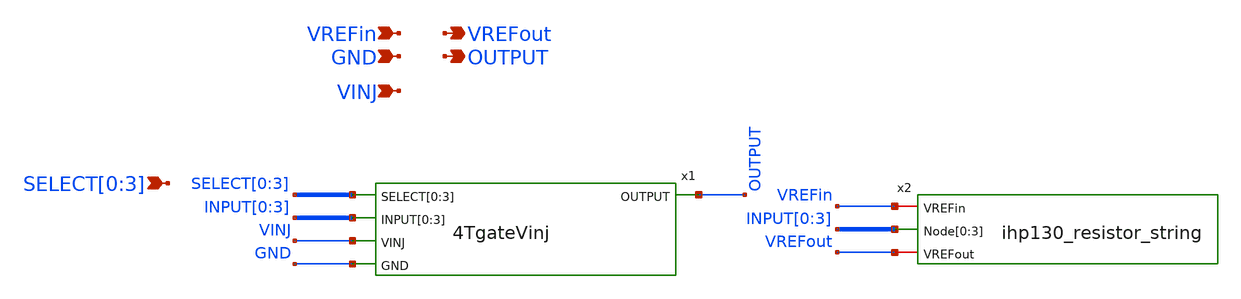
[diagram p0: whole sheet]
** sch_path: ihp130_cells/DAC_Cell/ihp130_DAC_cell.sch
**.subckt ihp130_DAC_cell GND VINJ SELECT[0],SELECT[1],SELECT[2],SELECT[3] VREFin VREFout OUTPUT
*.ipin GND
*.ipin VINJ
*.ipin SELECT[0],SELECT[1],SELECT[2],SELECT[3]
*.ipin VREFin
*.opin VREFout
*.opin OUTPUT
x1 SELECT[0] SELECT[1] SELECT[2] SELECT[3] OUTPUT INPUT[0] INPUT[1] INPUT[2] INPUT[3] VINJ GND
+ 4TgateVinj
x2 VREFin INPUT[0] INPUT[1] INPUT[2] INPUT[3] VREFout ihp130_resistor_string
**.ends

* expanding   symbol:  4TgateVinj/4TgateVinj.sym # of pins=5
** sym_path: ihp130_cells/4TgateVinj/4TgateVinj.sym
** sch_path: ihp130_cells/4TgateVinj/4TgateVinj.sch
.subckt 4TgateVinj SELECT[0] SELECT[1] SELECT[2] SELECT[3] OUTPUT INPUT[0] INPUT[1] INPUT[2]
+ INPUT[3] VINJ GND
*.ipin SELECT[0],SELECT[1],SELECT[2],SELECT[3]
*.ipin INPUT[0],INPUT[1],INPUT[2],INPUT[3]
*.ipin VINJ
*.ipin GND
*.opin OUTPUT
x1 SELECT[0] INPUT[0] VINJ GND OUTPUT ihp130_TgateVinj02
x2 SELECT[1] INPUT[1] VINJ GND OUTPUT ihp130_TgateVinj02
x3 SELECT[2] INPUT[2] VINJ GND OUTPUT ihp130_TgateVinj02
x4 SELECT[3] INPUT[3] VINJ GND OUTPUT ihp130_TgateVinj02
.ends


* expanding   symbol:  Resistor_String/ihp130_resistor_string.sym # of pins=3
** sym_path: ihp130_cells/Resistor_String/ihp130_resistor_string.sym
** sch_path: ihp130_cells/Resistor_String/ihp130_resistor_string.sch
.subckt ihp130_resistor_string VREFin Node[0] Node[1] Node[2] Node[3] VREFout
*.iopin VREFout
*.iopin VREFin
*.opin Node[0],Node[1],Node[2],Node[3]
XR8 VREFin Node[0] sub! rsil w=.59e-6 l=10e-6 m=1 mm_ok=1
XR1 Node[0] net1 sub! rsil w=.59e-6 l=10e-6 m=1 mm_ok=1
XR2 net1 Node[1] sub! rsil w=.59e-6 l=10e-6 m=1 mm_ok=1
XR3 Node[1] net2 sub! rsil w=.59e-6 l=10e-6 m=1 mm_ok=1
XR4 net2 Node[2] sub! rsil w=.59e-6 l=10e-6 m=1 mm_ok=1
XR5 Node[2] net3 sub! rsil w=.59e-6 l=10e-6 m=1 mm_ok=1
XR6 net3 Node[3] sub! rsil w=.59e-6 l=10e-6 m=1 mm_ok=1
XR7 Node[3] VREFout sub! rsil w=.59e-6 l=10e-6 m=1 mm_ok=1
.ends


* expanding   symbol:  TgateVinj02/ihp130_TgateVinj02.sym # of pins=5
** sym_path: ihp130_cells/TgateVinj02/ihp130_TgateVinj02.sym
** sch_path: ihp130_cells/TgateVinj02/ihp130_TgateVinj02.sch
.subckt ihp130_TgateVinj02 SELECT INPUT VINJ GND OUTPUT
*.ipin SELECT
*.ipin INPUT
*.ipin VINJ
*.ipin GND
*.opin OUTPUT
XM1 Selb SELECT VINJ VINJ sg13_hv_pmos w=0.42u l=0.5u ng=1 m=1 mm_ok=1
XM2 Selb SELECT GND GND sg13_hv_nmos w=0.42u l=0.5u ng=1 m=1 mm_ok=1
XM3 INPUT Selb OUTPUT VINJ sg13_hv_pmos w=0.42u l=0.5u ng=1 m=1 mm_ok=1
XM4 INPUT SELECT OUTPUT GND sg13_hv_nmos w=0.42u l=0.5u ng=1 m=1 mm_ok=1
.ends

.end
